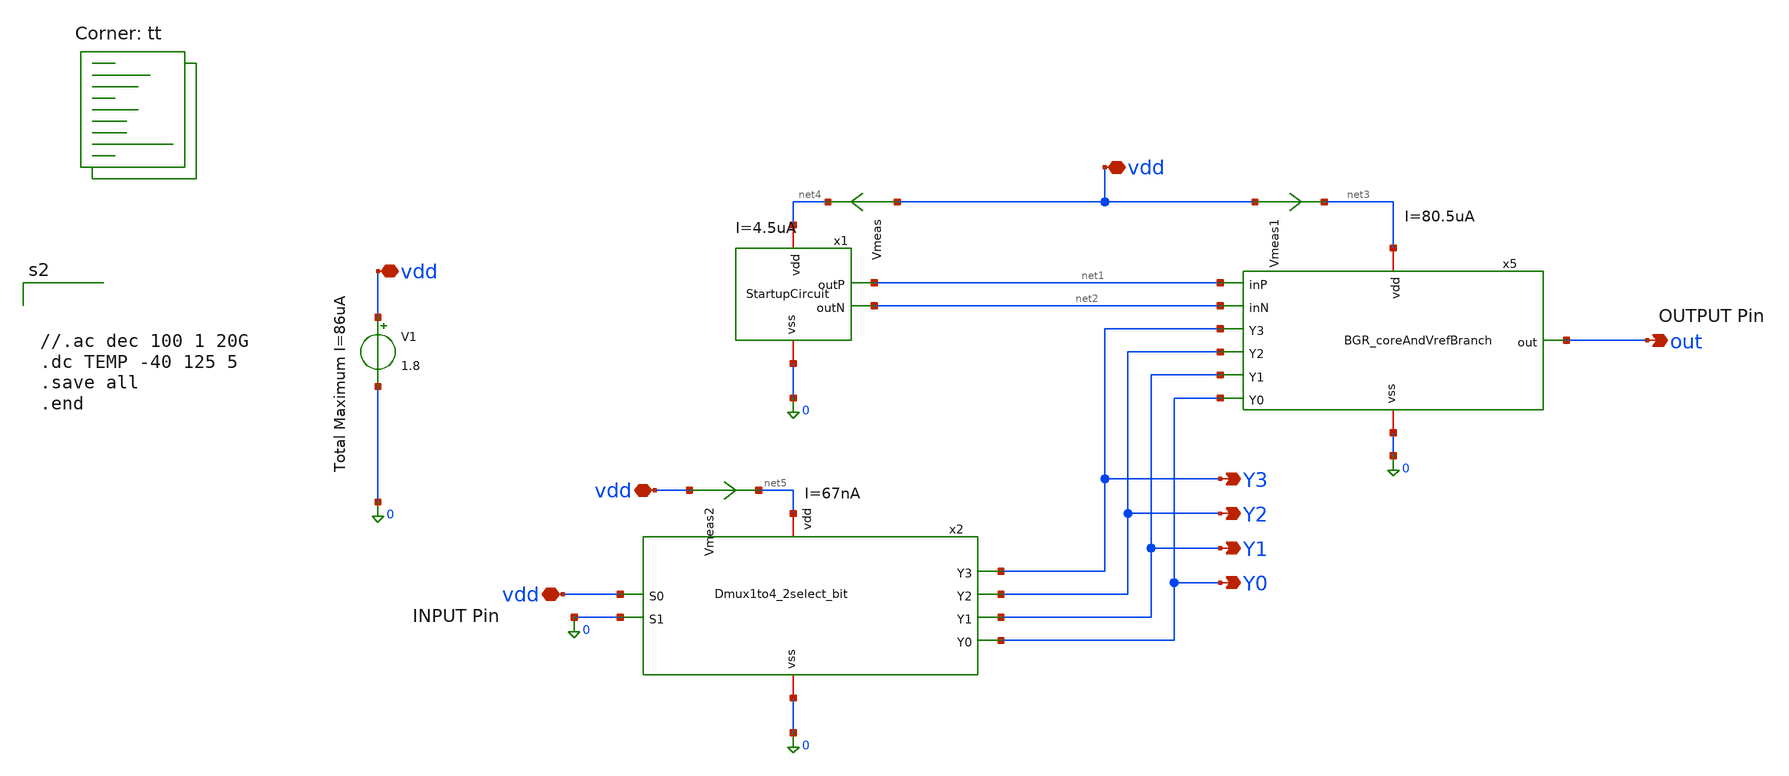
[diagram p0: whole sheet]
** sch_path: TB_BGR_v3.sch
**.subckt TB_BGR_v3 vdd vdd vdd vdd out Y3 Y2 Y1 Y0
*.iopin vdd
*.iopin vdd
*.iopin vdd
*.iopin vdd
*.opin out
*.opin Y3
*.opin Y2
*.opin Y1
*.opin Y0
x1 net4 net1 net2 0 StartupCircuit
V1 vdd 0 1.8
x5 net3 net1 out net2 Y3 Y2 Y1 Y0 0 BGR_coreAndVrefBranch
x2 net5 vdd 0 0 Y3 Y2 Y1 Y0 Dmux1to4_2select_bit
Vmeas vdd net4 0
.save i(vmeas)
Vmeas1 vdd net3 0
.save i(vmeas1)
Vmeas2 vdd net5 0
.save i(vmeas2)
**** begin user architecture code
.lib $::SKYWATER_MODELS/sky130.lib.spice tt



//.ac dec 100 1 20G
.dc TEMP -40 125 5
.save all
.end


**** end user architecture code
**.ends

* expanding   symbol:  StartupCircuit.sym # of pins=4
** sym_path: BGR_TOP_SKY130A/StartupCircuit.sym
** sch_path: BGR_TOP_SKY130A/StartupCircuit.sch
.subckt StartupCircuit vdd outP outN vss
*.iopin vdd
*.iopin vss
*.opin outP
*.opin outN
XM4 net2 outP vdd vdd sky130_fd_pr__pfet_01v8_lvt L=1 W=2 nf=1 ad='int((1 + 1)/2) * 2 / 1 * 0.29' as='int((1 + 2)/2) * 2 / 1 * 0.29'
+ pd='2*int((1 + 1)/2) * (2 / 1 + 0.29)' ps='2*int((1 + 2)/2) * (2 / 1 + 0.29)' nrd='0.29 / 2 ' nrs='0.29 / 2 '
+ sa=0 sb=0 sd=0 mult=1 m=1
XM7 outN net1 outP vdd sky130_fd_pr__pfet_01v8_lvt L=1 W=2 nf=1 ad='int((1 + 1)/2) * 2 / 1 * 0.29' as='int((1 + 2)/2) * 2 / 1 * 0.29'
+ pd='2*int((1 + 1)/2) * (2 / 1 + 0.29)' ps='2*int((1 + 2)/2) * (2 / 1 + 0.29)' nrd='0.29 / 2 ' nrs='0.29 / 2 '
+ sa=0 sb=0 sd=0 mult=2 m=2
XM9 net1 net1 net3 vss sky130_fd_pr__nfet_01v8_lvt L=1 W=1 nf=1 ad='int((1 + 1)/2) * 1 / 1 * 0.29' as='int((1 + 2)/2) * 1 / 1 * 0.29'
+ pd='2*int((1 + 1)/2) * (1 / 1 + 0.29)' ps='2*int((1 + 2)/2) * (1 / 1 + 0.29)' nrd='0.29 / 1 ' nrs='0.29 / 1 '
+ sa=0 sb=0 sd=0 mult=1 m=1
XM5 net1 outP net2 vdd sky130_fd_pr__pfet_01v8_lvt L=1 W=2 nf=1 ad='int((1 + 1)/2) * 2 / 1 * 0.29' as='int((1 + 2)/2) * 2 / 1 * 0.29'
+ pd='2*int((1 + 1)/2) * (2 / 1 + 0.29)' ps='2*int((1 + 2)/2) * (2 / 1 + 0.29)' nrd='0.29 / 2 ' nrs='0.29 / 2 '
+ sa=0 sb=0 sd=0 mult=1 m=1
XM10 net3 net3 vss vss sky130_fd_pr__nfet_01v8_lvt L=1 W=1 nf=1 ad='int((1 + 1)/2) * 1 / 1 * 0.29' as='int((1 + 2)/2) * 1 / 1 * 0.29'
+ pd='2*int((1 + 1)/2) * (1 / 1 + 0.29)' ps='2*int((1 + 2)/2) * (1 / 1 + 0.29)' nrd='0.29 / 1 ' nrs='0.29 / 1 '
+ sa=0 sb=0 sd=0 mult=1 m=1
.ends


* expanding   symbol:  BGR_coreAndVrefBranch.sym # of pins=9
** sym_path: BGR_coreAndVrefBranch.sym
** sch_path: BGR_coreAndVrefBranch.sch
.subckt BGR_coreAndVrefBranch vdd inP out inN Y3 Y2 Y1 Y0 vss
*.opin out
*.iopin vss
*.ipin Y3
*.ipin Y2
*.ipin Y1
*.ipin Y0
*.iopin vdd
*.ipin inP
*.ipin inN
XM3 out inP vdd vdd sky130_fd_pr__pfet_01v8_lvt L=2 W=3.2 nf=1 ad='int((1 + 1)/2) * 3.2 / 1 * 0.29' as='int((1 + 2)/2) * 3.2 / 1 * 0.29'
+ pd='2*int((1 + 1)/2) * (3.2 / 1 + 0.29)' ps='2*int((1 + 2)/2) * (3.2 / 1 + 0.29)' nrd='0.29 / 3.2 ' nrs='0.29 / 3.2 '
+ sa=0 sb=0 sd=0 mult=4 m=4
XQ3 vss vss net1 sky130_fd_pr__pnp_05v5_W3p40L3p40 m=8
XR2 net1 net3 vss sky130_fd_pr__res_high_po W=0.22 L=8 mult=1 m=1
XM11 net3 Y3 out vdd sky130_fd_pr__pfet_01v8_lvt L=1 W=5 nf=1 ad='int((1 + 1)/2) * 5 / 1 * 0.29' as='int((1 + 2)/2) * 5 / 1 * 0.29'
+ pd='2*int((1 + 1)/2) * (5 / 1 + 0.29)' ps='2*int((1 + 2)/2) * (5 / 1 + 0.29)' nrd='0.29 / 5 ' nrs='0.29 / 5 '
+ sa=0 sb=0 sd=0 mult=8 m=8
XM12 net3 Y2 net4 vdd sky130_fd_pr__pfet_01v8_lvt L=1 W=5 nf=1 ad='int((1 + 1)/2) * 5 / 1 * 0.29' as='int((1 + 2)/2) * 5 / 1 * 0.29'
+ pd='2*int((1 + 1)/2) * (5 / 1 + 0.29)' ps='2*int((1 + 2)/2) * (5 / 1 + 0.29)' nrd='0.29 / 5 ' nrs='0.29 / 5 '
+ sa=0 sb=0 sd=0 mult=8 m=8
XM13 net3 Y1 net5 vdd sky130_fd_pr__pfet_01v8_lvt L=1 W=5 nf=1 ad='int((1 + 1)/2) * 5 / 1 * 0.29' as='int((1 + 2)/2) * 5 / 1 * 0.29'
+ pd='2*int((1 + 1)/2) * (5 / 1 + 0.29)' ps='2*int((1 + 2)/2) * (5 / 1 + 0.29)' nrd='0.29 / 5 ' nrs='0.29 / 5 '
+ sa=0 sb=0 sd=0 mult=8 m=8
XM14 net3 Y0 net2 vdd sky130_fd_pr__pfet_01v8_lvt L=1 W=5 nf=1 ad='int((1 + 1)/2) * 5 / 1 * 0.29' as='int((1 + 2)/2) * 5 / 1 * 0.29'
+ pd='2*int((1 + 1)/2) * (5 / 1 + 0.29)' ps='2*int((1 + 2)/2) * (5 / 1 + 0.29)' nrd='0.29 / 5 ' nrs='0.29 / 5 '
+ sa=0 sb=0 sd=0 mult=8 m=8
XR1 net2 net5 vss sky130_fd_pr__res_high_po W=1 L=0.5 mult=1 m=1
XR3 net5 net4 vss sky130_fd_pr__res_high_po W=2.304 L=0.5 mult=1 m=1
XR4 net4 out vss sky130_fd_pr__res_high_po W=2.147 L=0.5 mult=1 m=1
XM6 inN inN net8 vss sky130_fd_pr__nfet_01v8_lvt L=1 W=3.8 nf=1 ad='int((1 + 1)/2) * 3.8 / 1 * 0.29'
+ as='int((1 + 2)/2) * 3.8 / 1 * 0.29' pd='2*int((1 + 1)/2) * (3.8 / 1 + 0.29)' ps='2*int((1 + 2)/2) * (3.8 / 1 + 0.29)'
+ nrd='0.29 / 3.8 ' nrs='0.29 / 3.8 ' sa=0 sb=0 sd=0 mult=8 m=8
XM1 inN inP vdd vdd sky130_fd_pr__pfet_01v8_lvt L=2 W=3.2 nf=1 ad='int((1 + 1)/2) * 3.2 / 1 * 0.29' as='int((1 + 2)/2) * 3.2 / 1 * 0.29'
+ pd='2*int((1 + 1)/2) * (3.2 / 1 + 0.29)' ps='2*int((1 + 2)/2) * (3.2 / 1 + 0.29)' nrd='0.29 / 3.2 ' nrs='0.29 / 3.2 '
+ sa=0 sb=0 sd=0 mult=4 m=4
XQ1 vss vss net7 sky130_fd_pr__pnp_05v5_W3p40L3p40 m=8
XR5 net7 net6 vss sky130_fd_pr__res_high_po W=1.1 L=14.6 mult=1 m=1
XM2 inP inP vdd vdd sky130_fd_pr__pfet_01v8_lvt L=2 W=3.2 nf=1 ad='int((1 + 1)/2) * 3.2 / 1 * 0.29' as='int((1 + 2)/2) * 3.2 / 1 * 0.29'
+ pd='2*int((1 + 1)/2) * (3.2 / 1 + 0.29)' ps='2*int((1 + 2)/2) * (3.2 / 1 + 0.29)' nrd='0.29 / 3.2 ' nrs='0.29 / 3.2 '
+ sa=0 sb=0 sd=0 mult=4 m=4
XM8 inP inN net6 vss sky130_fd_pr__nfet_01v8_lvt L=1 W=3.8 nf=1 ad='int((1 + 1)/2) * 3.8 / 1 * 0.29'
+ as='int((1 + 2)/2) * 3.8 / 1 * 0.29' pd='2*int((1 + 1)/2) * (3.8 / 1 + 0.29)' ps='2*int((1 + 2)/2) * (3.8 / 1 + 0.29)'
+ nrd='0.29 / 3.8 ' nrs='0.29 / 3.8 ' sa=0 sb=0 sd=0 mult=8 m=8
XQ2 vss vss net9 sky130_fd_pr__pnp_05v5_W3p40L3p40 m=1
XR6 net9 net8 vss sky130_fd_pr__res_high_po W=2.28 L=14.6 mult=1 m=1
.ends


* expanding   symbol:  Dmux1to4_2select_bit.sym # of pins=8
** sym_path: Dmux1to4_2select_bit.sym
** sch_path: Dmux1to4_2select_bit.sch
.subckt Dmux1to4_2select_bit vdd S0 S1 vss Y3 Y2 Y1 Y0
*.ipin S0
*.ipin S1
*.iopin vdd
*.iopin vss
*.opin Y3
*.opin Y2
*.opin Y1
*.opin Y0
x1 vdd Y3 vdd S0 S1 vss NAND
x2 vdd S1 net2 vss NOT
x3 vdd S0 net1 vss NOT
x4 vdd Y2 vdd net1 S1 vss NAND
x5 vdd Y1 vdd S0 net2 vss NAND
x6 vdd Y0 vdd net1 net2 vss NAND
.ends


* expanding   symbol:  NAND.sym # of pins=6
** sym_path: NAND.sym
** sch_path: NAND.sch
.subckt NAND vdd out A B C vss
*.iopin vdd
*.iopin vss
*.ipin A
*.ipin C
*.ipin B
*.opin out
XM6 out A net1 vss sky130_fd_pr__nfet_01v8_lvt L=1 W=1 nf=1 ad='int((1 + 1)/2) * 1 / 1 * 0.29' as='int((1 + 2)/2) * 1 / 1 * 0.29'
+ pd='2*int((1 + 1)/2) * (1 / 1 + 0.29)' ps='2*int((1 + 2)/2) * (1 / 1 + 0.29)' nrd='0.29 / 1 ' nrs='0.29 / 1 '
+ sa=0 sb=0 sd=0 mult=2 m=2
XM1 out B vdd vdd sky130_fd_pr__pfet_01v8_lvt L=1 W=1 nf=1 ad='int((1 + 1)/2) * 1 / 1 * 0.29' as='int((1 + 2)/2) * 1 / 1 * 0.29'
+ pd='2*int((1 + 1)/2) * (1 / 1 + 0.29)' ps='2*int((1 + 2)/2) * (1 / 1 + 0.29)' nrd='0.29 / 1 ' nrs='0.29 / 1 '
+ sa=0 sb=0 sd=0 mult=4 m=4
XM2 out A vdd vdd sky130_fd_pr__pfet_01v8_lvt L=1 W=1 nf=1 ad='int((1 + 1)/2) * 1 / 1 * 0.29' as='int((1 + 2)/2) * 1 / 1 * 0.29'
+ pd='2*int((1 + 1)/2) * (1 / 1 + 0.29)' ps='2*int((1 + 2)/2) * (1 / 1 + 0.29)' nrd='0.29 / 1 ' nrs='0.29 / 1 '
+ sa=0 sb=0 sd=0 mult=4 m=4
XM3 net1 B net2 vss sky130_fd_pr__nfet_01v8_lvt L=1 W=1 nf=1 ad='int((1 + 1)/2) * 1 / 1 * 0.29' as='int((1 + 2)/2) * 1 / 1 * 0.29'
+ pd='2*int((1 + 1)/2) * (1 / 1 + 0.29)' ps='2*int((1 + 2)/2) * (1 / 1 + 0.29)' nrd='0.29 / 1 ' nrs='0.29 / 1 '
+ sa=0 sb=0 sd=0 mult=2 m=2
XM4 out C vdd vdd sky130_fd_pr__pfet_01v8_lvt L=1 W=1 nf=1 ad='int((1 + 1)/2) * 1 / 1 * 0.29' as='int((1 + 2)/2) * 1 / 1 * 0.29'
+ pd='2*int((1 + 1)/2) * (1 / 1 + 0.29)' ps='2*int((1 + 2)/2) * (1 / 1 + 0.29)' nrd='0.29 / 1 ' nrs='0.29 / 1 '
+ sa=0 sb=0 sd=0 mult=4 m=4
XM5 net2 C vss vss sky130_fd_pr__nfet_01v8_lvt L=1 W=1 nf=1 ad='int((1 + 1)/2) * 1 / 1 * 0.29' as='int((1 + 2)/2) * 1 / 1 * 0.29'
+ pd='2*int((1 + 1)/2) * (1 / 1 + 0.29)' ps='2*int((1 + 2)/2) * (1 / 1 + 0.29)' nrd='0.29 / 1 ' nrs='0.29 / 1 '
+ sa=0 sb=0 sd=0 mult=2 m=2
.ends


* expanding   symbol:  NOT.sym # of pins=4
** sym_path: NOT.sym
** sch_path: NOT.sch
.subckt NOT vdd in out vss
*.iopin vdd
*.iopin vss
*.ipin in
*.opin out
XM6 out in vss vss sky130_fd_pr__nfet_01v8_lvt L=1 W=1 nf=1 ad='int((1 + 1)/2) * 1 / 1 * 0.29' as='int((1 + 2)/2) * 1 / 1 * 0.29'
+ pd='2*int((1 + 1)/2) * (1 / 1 + 0.29)' ps='2*int((1 + 2)/2) * (1 / 1 + 0.29)' nrd='0.29 / 1 ' nrs='0.29 / 1 '
+ sa=0 sb=0 sd=0 mult=1 m=1
XM1 out in vdd vdd sky130_fd_pr__pfet_01v8_lvt L=1 W=1 nf=1 ad='int((1 + 1)/2) * 1 / 1 * 0.29' as='int((1 + 2)/2) * 1 / 1 * 0.29'
+ pd='2*int((1 + 1)/2) * (1 / 1 + 0.29)' ps='2*int((1 + 2)/2) * (1 / 1 + 0.29)' nrd='0.29 / 1 ' nrs='0.29 / 1 '
+ sa=0 sb=0 sd=0 mult=2 m=2
.ends

.end
